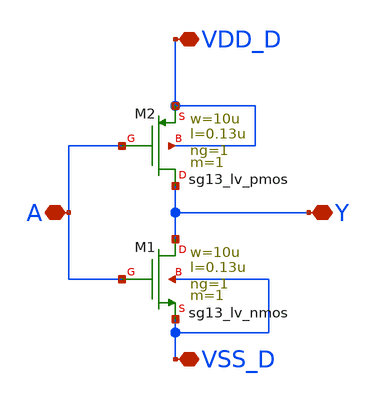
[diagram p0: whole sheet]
** sch_path: xschem/inv_1_manual/inv_1_manual.sch
**.subckt inv_1_manual VDD_D VSS_D A Y
*.iopin VDD_D
*.iopin VSS_D
*.iopin A
*.iopin Y
XM1 Y A VSS_D VSS_D sg13_lv_nmos w=10u l=0.13u ng=1 m=1 mm_ok=1
XM2 Y A VDD_D VDD_D sg13_lv_pmos w=10u l=0.13u ng=1 m=1 mm_ok=1
**.ends
.end
